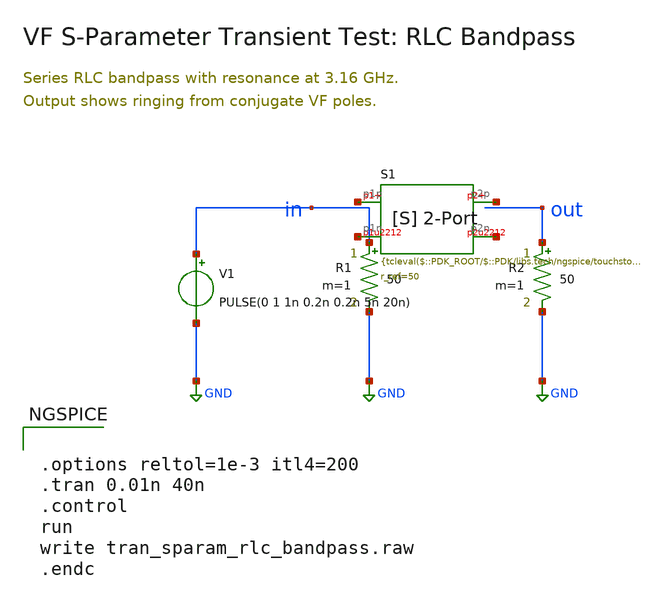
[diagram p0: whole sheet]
** sch_path: ihp-sg13g2/libs.tech/xschem/sg13g2_tests/tran_sparam_rlc_bandpass.sch
* Copyright 2024 IHP PDK Authors
**.subckt tran_sparam_rlc_bandpass
V1 in GND PULSE(0 1 1n 0.2n 0.2n 5n 20n)
R1 in GND 50 m=1
R2 out GND 50 m=1
AS1 [ net1 net2 net3 net4 ] bandpass_model
.model bandpass_model sparam( file=" r_ref=50 n_poles=0 vf_tol=1e-3 vf_maxiter=10 )
**** begin user architecture code


.options reltol=1e-3 itl4=200
.tran 0.01n 40n
.control
run
write tran_sparam_rlc_bandpass.raw
.endc


**** end user architecture code
**.ends
.GLOBAL GND
.end
